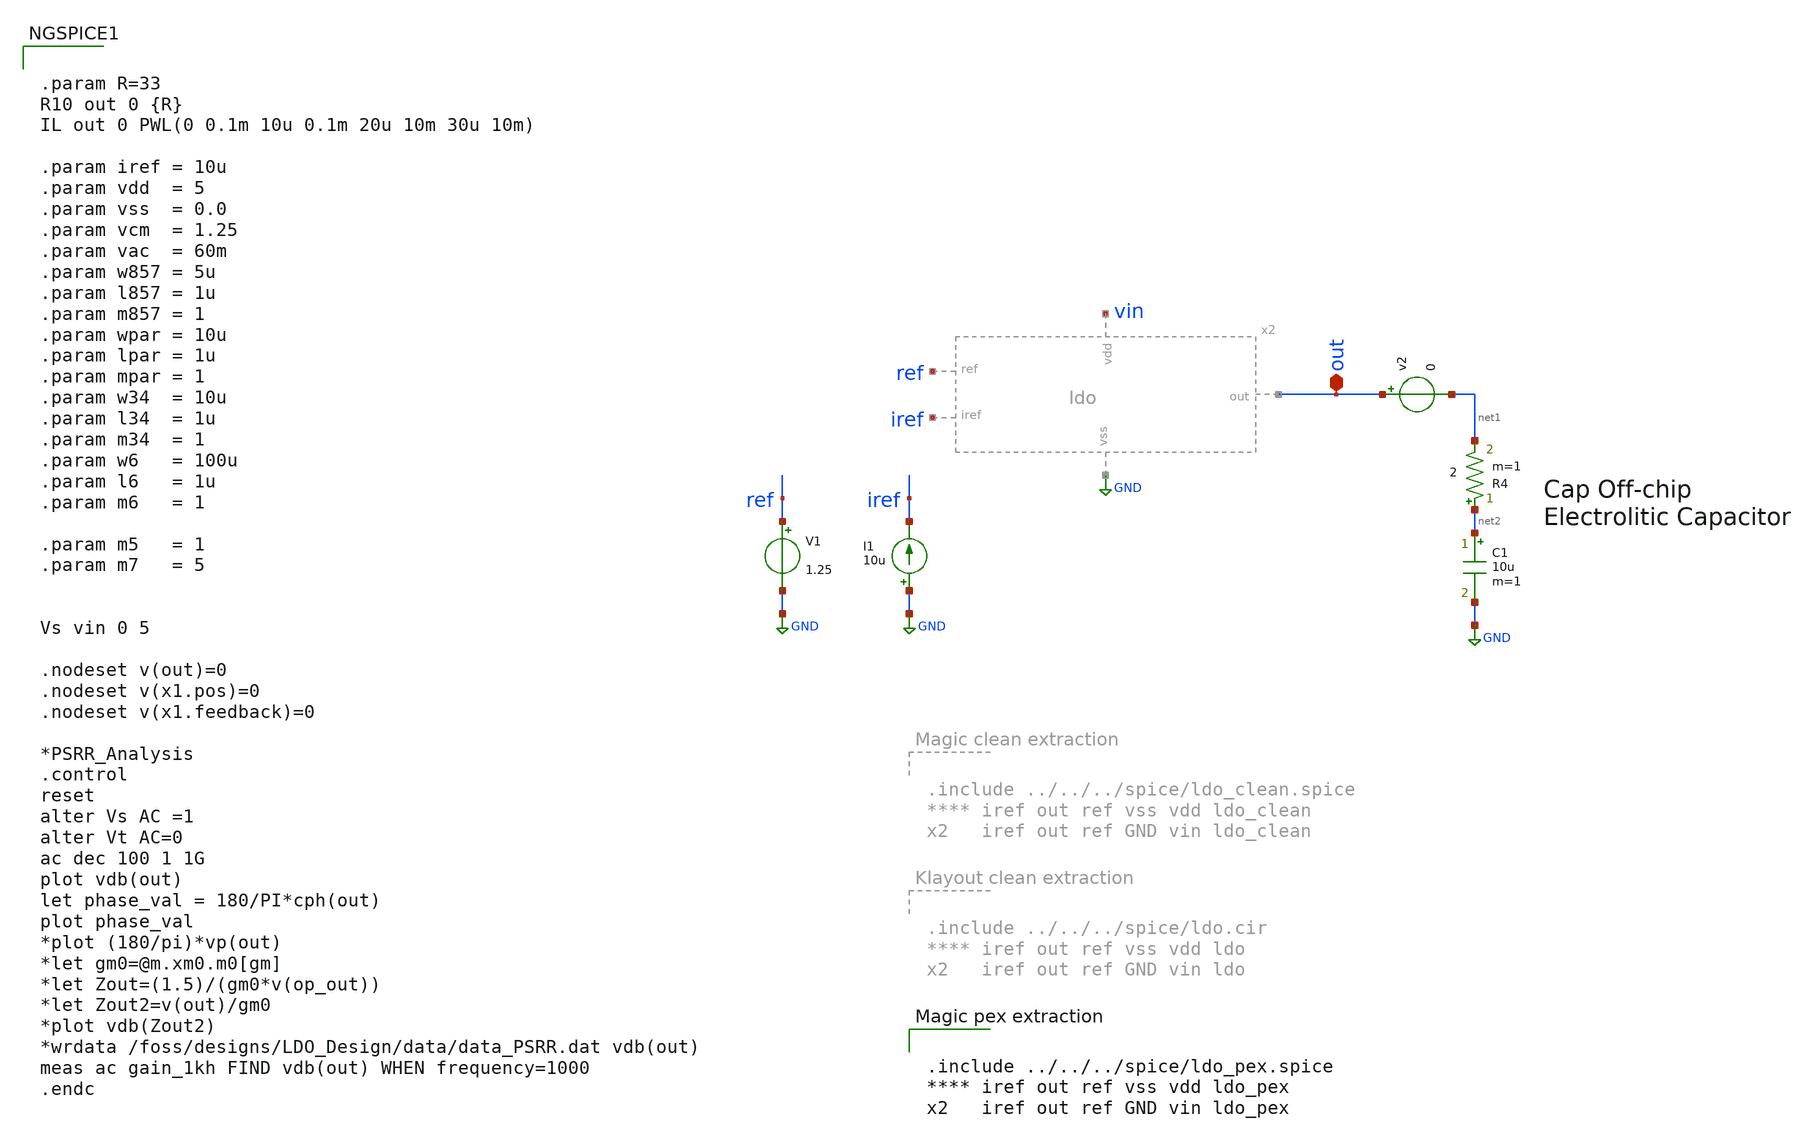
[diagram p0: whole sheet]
** sch_path: LDO/xschem/ldo/test/psrr.sch

.include $env(PDK_ROOT)/$env(PDK)/libs.tech/ngspice/design.ngspice
.lib $env(PDK_ROOT)/$env(PDK)/libs.tech/ngspice/sm141064.ngspice typical
.lib $env(PDK_ROOT)/$env(PDK)/libs.tech/ngspice/sm141064.ngspice res_typical

.lib $env(PDK_ROOT)/$env(PDK)/libs.tech/ngspice/sm141064.ngspice cap_mim
.lib $env(PDK_ROOT)/$env(PDK)/libs.tech/ngspice/sm141064.ngspice mimcap_typical

**.subckt psrr out
*.iopin out
I1 GND iref 10u
V1 ref GND 1.25
v2 out net1 0
C1 net2 GND 10u m=1
R4 net2 net1 2 m=1
**** begin user architecture code


.param R=33
R10 out 0 {R}
IL out 0 PWL(0 0.1m 10u 0.1m 20u 10m 30u 10m)

.param iref = 10u
.param vdd  = 5
.param vss  = 0.0
.param vcm  = 1.25
.param vac  = 60m
.param w857 = 5u
.param l857 = 1u
.param m857 = 1
.param wpar = 10u
.param lpar = 1u
.param mpar = 1
.param w34  = 10u
.param l34  = 1u
.param m34  = 1
.param w6   = 100u
.param l6   = 1u
.param m6   = 1

.param m5   = 1
.param m7   = 5


Vs vin 0 5

.nodeset v(out)=0
.nodeset v(x1.pos)=0
.nodeset v(x1.feedback)=0

*PSRR_Analysis
.control
reset
alter Vs AC =1
alter Vt AC=0
ac dec 100 1 1G
plot vdb(out)
let phase_val = 180/PI*cph(out)
plot phase_val
*plot (180/pi)*vp(out)
*let gm0=@m.xm0.m0[gm]
*let Zout=(1.5)/(gm0*v(op_out))
*let Zout2=v(out)/gm0
*plot vdb(Zout2)
*wrdata /foss/designs/LDO_Design/data/data_PSRR.dat vdb(out)
meas ac gain_1kh FIND vdb(out) WHEN frequency=1000
.endc




.include ../../../spice/ldo_pex.spice
**** iref out ref vss vdd ldo_pex
x2   iref out ref GND vin ldo_pex


**** end user architecture code
**.ends
.GLOBAL GND
.end
